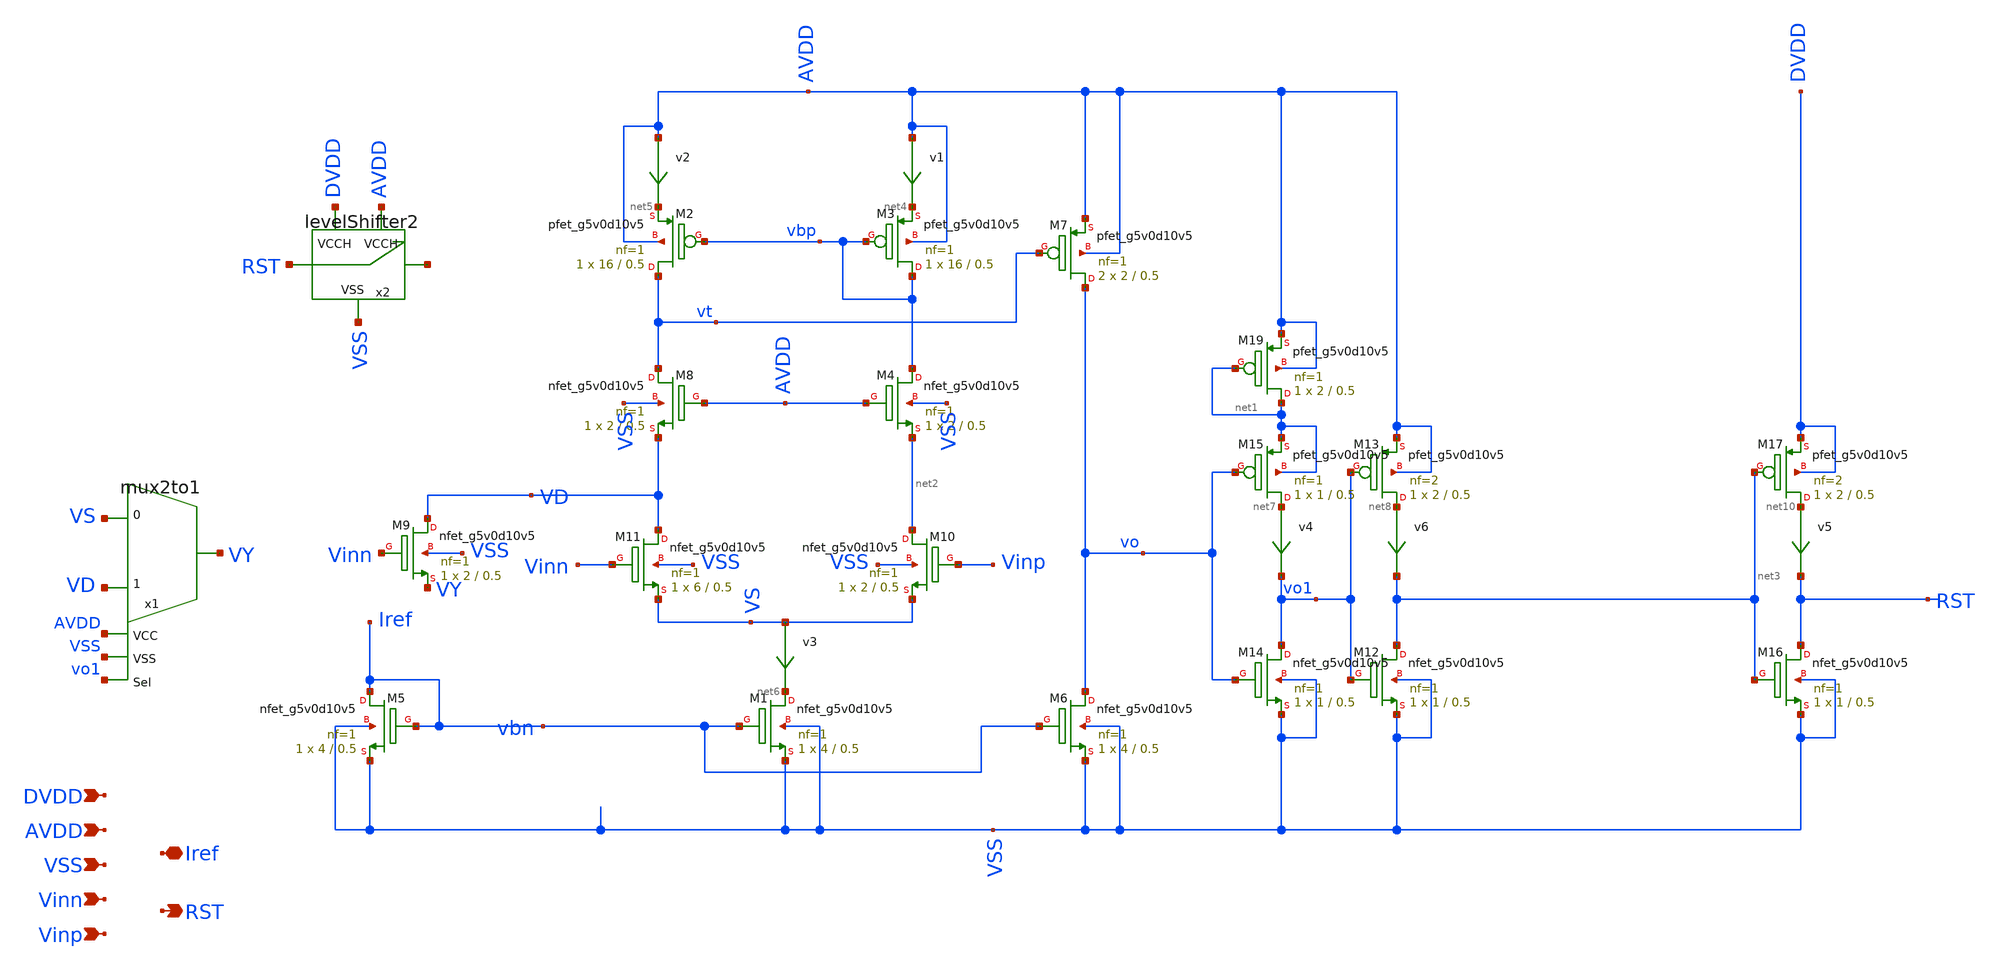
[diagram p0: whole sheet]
** sch_path: xschem_sim/comparator.sch
**.subckt comparator AVDD RST VSS Iref Vinn Vinp DVDD
*.ipin AVDD
*.opin RST
*.ipin VSS
*.iopin Iref
*.ipin Vinn
*.ipin Vinp
*.ipin DVDD
v1 AVDD net4 0
.save i(v1)
v2 AVDD net5 0
.save i(v2)
XM1 net6 Iref VSS VSS sky130_fd_pr__nfet_g5v0d10v5 L=0.5 W=4 nf=1 ad='int((nf+1)/2) * W/nf * 0.29' as='int((nf+2)/2) * W/nf * 0.29'
+ pd='2*int((nf+1)/2) * (W/nf + 0.29)' ps='2*int((nf+2)/2) * (W/nf + 0.29)' nrd='0.29 / W' nrs='0.29 / W'
+ sa=0 sb=0 sd=0 mult=1 m=1
XM3 vbp vbp net4 AVDD sky130_fd_pr__pfet_g5v0d10v5 L=0.5 W=16 nf=1 ad='int((nf+1)/2) * W/nf * 0.29' as='int((nf+2)/2) * W/nf * 0.29'
+ pd='2*int((nf+1)/2) * (W/nf + 0.29)' ps='2*int((nf+2)/2) * (W/nf + 0.29)' nrd='0.29 / W' nrs='0.29 / W'
+ sa=0 sb=0 sd=0 mult=1 m=1
XM2 vt vbp net5 AVDD sky130_fd_pr__pfet_g5v0d10v5 L=0.5 W=16 nf=1 ad='int((nf+1)/2) * W/nf * 0.29' as='int((nf+2)/2) * W/nf * 0.29'
+ pd='2*int((nf+1)/2) * (W/nf + 0.29)' ps='2*int((nf+2)/2) * (W/nf + 0.29)' nrd='0.29 / W' nrs='0.29 / W'
+ sa=0 sb=0 sd=0 mult=1 m=1
v4 net7 vo1 0
.save i(v4)
XM9 VD Vinn VY VSS sky130_fd_pr__nfet_g5v0d10v5 L=0.5 W=2 nf=1 ad='int((nf+1)/2) * W/nf * 0.29' as='int((nf+2)/2) * W/nf * 0.29'
+ pd='2*int((nf+1)/2) * (W/nf + 0.29)' ps='2*int((nf+2)/2) * (W/nf + 0.29)' nrd='0.29 / W' nrs='0.29 / W'
+ sa=0 sb=0 sd=0 mult=1 m=1
XM10 net2 Vinp VS VSS sky130_fd_pr__nfet_g5v0d10v5 L=0.5 W=2 nf=1 ad='int((nf+1)/2) * W/nf * 0.29' as='int((nf+2)/2) * W/nf * 0.29'
+ pd='2*int((nf+1)/2) * (W/nf + 0.29)' ps='2*int((nf+2)/2) * (W/nf + 0.29)' nrd='0.29 / W' nrs='0.29 / W'
+ sa=0 sb=0 sd=0 mult=1 m=1
XM5 Iref Iref VSS VSS sky130_fd_pr__nfet_g5v0d10v5 L=0.5 W=4 nf=1 ad='int((nf+1)/2) * W/nf * 0.29' as='int((nf+2)/2) * W/nf * 0.29'
+ pd='2*int((nf+1)/2) * (W/nf + 0.29)' ps='2*int((nf+2)/2) * (W/nf + 0.29)' nrd='0.29 / W' nrs='0.29 / W'
+ sa=0 sb=0 sd=0 mult=1 m=1
XM7 vo vt AVDD AVDD sky130_fd_pr__pfet_g5v0d10v5 L=0.5 W=2 nf=1 ad='int((nf+1)/2) * W/nf * 0.29' as='int((nf+2)/2) * W/nf * 0.29'
+ pd='2*int((nf+1)/2) * (W/nf + 0.29)' ps='2*int((nf+2)/2) * (W/nf + 0.29)' nrd='0.29 / W' nrs='0.29 / W'
+ sa=0 sb=0 sd=0 mult=2 m=2
v3 VS net6 0
.save i(v3)
XM11 VD Vinn VS VSS sky130_fd_pr__nfet_g5v0d10v5 L=0.5 W=6 nf=1 ad='int((nf+1)/2) * W/nf * 0.29' as='int((nf+2)/2) * W/nf * 0.29'
+ pd='2*int((nf+1)/2) * (W/nf + 0.29)' ps='2*int((nf+2)/2) * (W/nf + 0.29)' nrd='0.29 / W' nrs='0.29 / W'
+ sa=0 sb=0 sd=0 mult=1 m=1
x1 VD VS VY AVDD VSS vo1 mux2to1
XM6 vo Iref VSS VSS sky130_fd_pr__nfet_g5v0d10v5 L=0.5 W=4 nf=1 ad='int((nf+1)/2) * W/nf * 0.29' as='int((nf+2)/2) * W/nf * 0.29'
+ pd='2*int((nf+1)/2) * (W/nf + 0.29)' ps='2*int((nf+2)/2) * (W/nf + 0.29)' nrd='0.29 / W' nrs='0.29 / W'
+ sa=0 sb=0 sd=0 mult=1 m=1
v6 net8 net3 0
.save i(v6)
XM14 vo1 vo VSS VSS sky130_fd_pr__nfet_g5v0d10v5 L=0.5 W=1 nf=1 ad='int((nf+1)/2) * W/nf * 0.29' as='int((nf+2)/2) * W/nf * 0.29'
+ pd='2*int((nf+1)/2) * (W/nf + 0.29)' ps='2*int((nf+2)/2) * (W/nf + 0.29)' nrd='0.29 / W' nrs='0.29 / W'
+ sa=0 sb=0 sd=0 mult=1 m=1
XM15 net7 vo net1 net1 sky130_fd_pr__pfet_g5v0d10v5 L=0.5 W=1 nf=1 ad='int((nf+1)/2) * W/nf * 0.29' as='int((nf+2)/2) * W/nf * 0.29'
+ pd='2*int((nf+1)/2) * (W/nf + 0.29)' ps='2*int((nf+2)/2) * (W/nf + 0.29)' nrd='0.29 / W' nrs='0.29 / W'
+ sa=0 sb=0 sd=0 mult=1 m=1
XM12 net3 vo1 VSS VSS sky130_fd_pr__nfet_g5v0d10v5 L=0.5 W=1 nf=1 ad='int((nf+1)/2) * W/nf * 0.29' as='int((nf+2)/2) * W/nf * 0.29'
+ pd='2*int((nf+1)/2) * (W/nf + 0.29)' ps='2*int((nf+2)/2) * (W/nf + 0.29)' nrd='0.29 / W' nrs='0.29 / W'
+ sa=0 sb=0 sd=0 mult=1 m=1
XM13 net8 vo1 AVDD AVDD sky130_fd_pr__pfet_g5v0d10v5 L=0.5 W=2 nf=2 ad='int((nf+1)/2) * W/nf * 0.29'
+ as='int((nf+2)/2) * W/nf * 0.29' pd='2*int((nf+1)/2) * (W/nf + 0.29)' ps='2*int((nf+2)/2) * (W/nf + 0.29)'
+ nrd='0.29 / W' nrs='0.29 / W' sa=0 sb=0 sd=0 mult=1 m=1
x2 RST net9 DVDD VSS AVDD levelShifter2
v5 net10 RST 0
.save i(v5)
XM16 RST net3 VSS VSS sky130_fd_pr__nfet_g5v0d10v5 L=0.5 W=1 nf=1 ad='int((nf+1)/2) * W/nf * 0.29' as='int((nf+2)/2) * W/nf * 0.29'
+ pd='2*int((nf+1)/2) * (W/nf + 0.29)' ps='2*int((nf+2)/2) * (W/nf + 0.29)' nrd='0.29 / W' nrs='0.29 / W'
+ sa=0 sb=0 sd=0 mult=1 m=1
XM17 net10 net3 DVDD DVDD sky130_fd_pr__pfet_g5v0d10v5 L=0.5 W=2 nf=2 ad='int((nf+1)/2) * W/nf * 0.29'
+ as='int((nf+2)/2) * W/nf * 0.29' pd='2*int((nf+1)/2) * (W/nf + 0.29)' ps='2*int((nf+2)/2) * (W/nf + 0.29)'
+ nrd='0.29 / W' nrs='0.29 / W' sa=0 sb=0 sd=0 mult=1 m=1
XM4 vbp AVDD net2 VSS sky130_fd_pr__nfet_g5v0d10v5 L=0.5 W=2 nf=1 ad='int((nf+1)/2) * W/nf * 0.29' as='int((nf+2)/2) * W/nf * 0.29'
+ pd='2*int((nf+1)/2) * (W/nf + 0.29)' ps='2*int((nf+2)/2) * (W/nf + 0.29)' nrd='0.29 / W' nrs='0.29 / W'
+ sa=0 sb=0 sd=0 mult=1 m=1
XM8 vt AVDD VD VSS sky130_fd_pr__nfet_g5v0d10v5 L=0.5 W=2 nf=1 ad='int((nf+1)/2) * W/nf * 0.29' as='int((nf+2)/2) * W/nf * 0.29'
+ pd='2*int((nf+1)/2) * (W/nf + 0.29)' ps='2*int((nf+2)/2) * (W/nf + 0.29)' nrd='0.29 / W' nrs='0.29 / W'
+ sa=0 sb=0 sd=0 mult=1 m=1
XM19 net1 net1 AVDD AVDD sky130_fd_pr__pfet_g5v0d10v5 L=0.5 W=2 nf=1 ad='int((nf+1)/2) * W/nf * 0.29'
+ as='int((nf+2)/2) * W/nf * 0.29' pd='2*int((nf+1)/2) * (W/nf + 0.29)' ps='2*int((nf+2)/2) * (W/nf + 0.29)'
+ nrd='0.29 / W' nrs='0.29 / W' sa=0 sb=0 sd=0 mult=1 m=1
**.ends
.end
